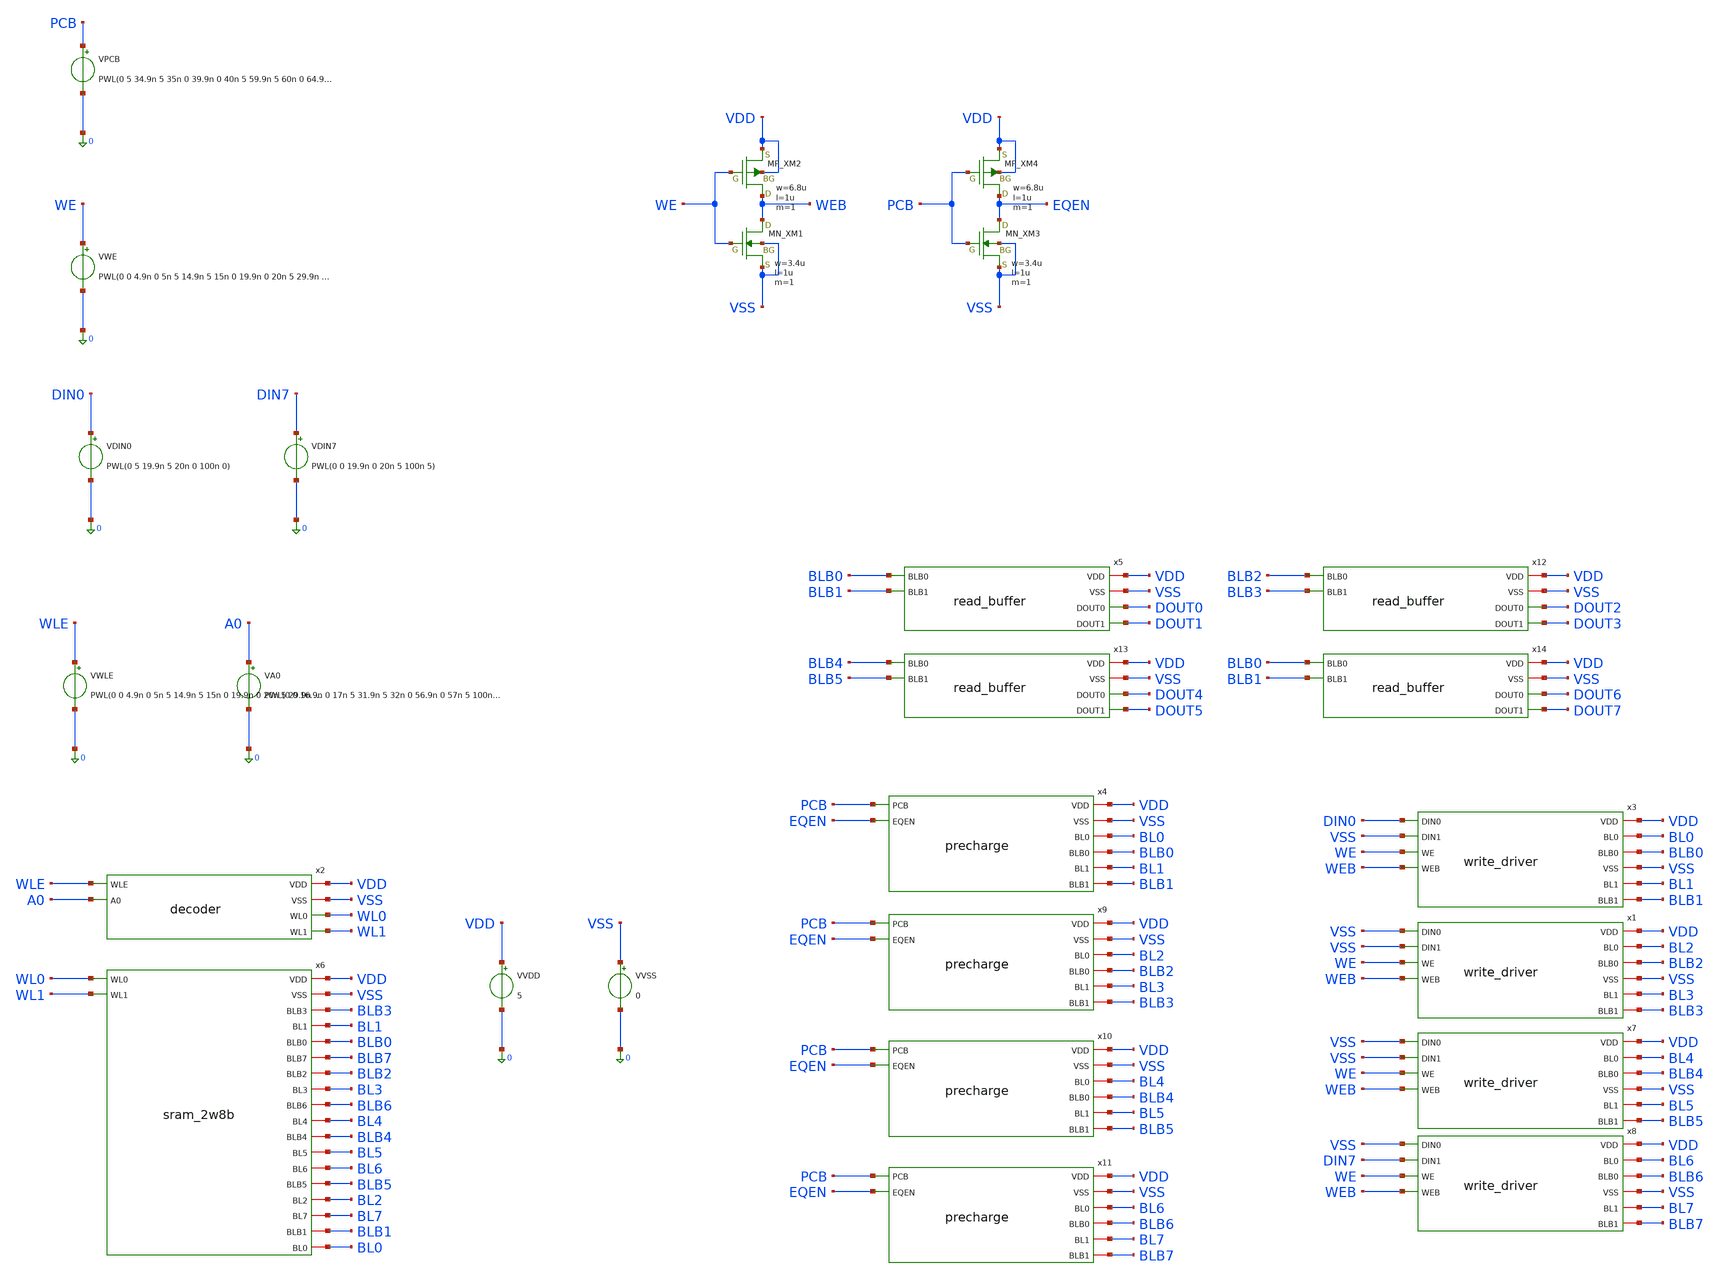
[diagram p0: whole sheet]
** sch_path: array/8word_x_2bit/tb_sram_2w8b.sch
**.subckt tb_sram_2w8b
VVDD VDD 0 5
VDIN0 DIN0 0 PWL(0 5 19.9n 5 20n 0 100n 0)
VVSS VSS 0 0
VWE WE 0 PWL(0 0 4.9n 0 5n 5 14.9n 5 15n 0 19.9n 0 20n 5 29.9n 5 30n 0 100n 0)
VPCB PCB 0 PWL(0 5 34.9n 5 35n 0 39.9n 0 40n 5 59.9n 5 60n 0 64.9n 0 65n 5 100n 5)
x2 VDD VSS WL0 WLE A0 WL1 decoder
VWLE WLE 0 PWL(0 0 4.9n 0 5n 5 14.9n 5 15n 0 19.9n 0 20n 5 29.9n 5 30n 0 44.9n 0 45n 5 54.9n 5 55n 0
+ 69.9n 0 70n 5 79.9n 5 80n 0 100n 0)
VA0 A0 0 PWL(0 0 16.9n 0 17n 5 31.9n 5 32n 0 56.9n 0 57n 5 100n 5)
x3 DIN0 VDD BL0 BLB0 VSS VSS BL1 WE BLB1 WEB write_driver
VDIN7 DIN7 0 PWL(0 0 19.9n 0 20n 5 100n 5)
x4 VDD VSS PCB EQEN BL0 BLB0 BL1 BLB1 precharge
x5 VDD VSS BLB0 BLB1 DOUT0 DOUT1 read_buffer
XXM1 WEB WE VSS VSS NMOS w=3.4u l=1u nrd=0 nrs=0 m=1
XXM2 WEB WE VDD VDD PMOS w=6.8u l=1u nrd=0 nrs=0 m=1
XXM3 EQEN PCB VSS VSS NMOS w=3.4u l=1u nrd=0 nrs=0 m=1
XXM4 EQEN PCB VDD VDD PMOS w=6.8u l=1u nrd=0 nrs=0 m=1
x6 WL0 VDD VSS WL1 BLB3 BL1 BLB0 BLB7 BLB2 BL3 BLB6 BL4 BLB4 BL5 BL6 BLB5 BL2 BL7 BLB1 BL0 sram_2w8b
x1 VSS VDD BL2 BLB2 VSS VSS BL3 WE BLB3 WEB write_driver
x7 VSS VDD BL4 BLB4 VSS VSS BL5 WE BLB5 WEB write_driver
x8 VSS VDD BL6 BLB6 VSS DIN7 BL7 WE BLB7 WEB write_driver
x9 VDD VSS PCB EQEN BL2 BLB2 BL3 BLB3 precharge
x10 VDD VSS PCB EQEN BL4 BLB4 BL5 BLB5 precharge
x11 VDD VSS PCB EQEN BL6 BLB6 BL7 BLB7 precharge
x12 VDD VSS BLB2 BLB3 DOUT2 DOUT3 read_buffer
x13 VDD VSS BLB4 BLB5 DOUT4 DOUT5 read_buffer
x14 VDD VSS BLB0 BLB1 DOUT6 DOUT7 read_buffer
**** begin user architecture code
 .include $::LIB/ip62_models


.tran 10p 100n

* ============================================================
* ColMax 2w8b SRAM Read Measurement
* Observe: bit1 and bit7
* ============================================================

* WL 50% crossing
.meas tran t_wl0_rise WHEN v(WL0)=2.5 RISE=2
.meas tran t_wl1_rise WHEN v(WL1)=2.5 RISE=1

* BL differential at WL0 +0.5ns
.meas tran dvbl1_05 FIND par('abs(v(BL1)-v(BLB1))') AT=47.781n
.meas tran dvbl7_05 FIND par('abs(v(BL7)-v(BLB7))') AT=47.781n

* BL differential at WL0 +1.0ns
.meas tran dvbl1_10 FIND par('abs(v(BL1)-v(BLB1))') AT=48.281n
.meas tran dvbl7_10 FIND par('abs(v(BL7)-v(BLB7))') AT=48.281n

* Time when BL differential reaches 1.0V
.meas tran t_dvbl1_1v WHEN par('abs(v(BL1)-v(BLB1))')=1.0 RISE=1 TD=47n
.meas tran t_dvbl7_1v WHEN par('abs(v(BL7)-v(BLB7))')=1.0 RISE=1 TD=47n

* Delay from WL0 50% to 1.0V BL differential
.meas tran td_bl1 PARAM='t_dvbl1_1v-t_wl0_rise'
.meas tran td_bl7 PARAM='t_dvbl7_1v-t_wl0_rise'

.control
run

plot v(pcb) v(eqen)+6
plot v(wl0) v(wl1)+6
plot v(dout1) v(dout7)+6
plot v(bl1) v(blb1)
plot v(bl7) v(blb7)

.endc


**** end user architecture code
**.ends
.end
